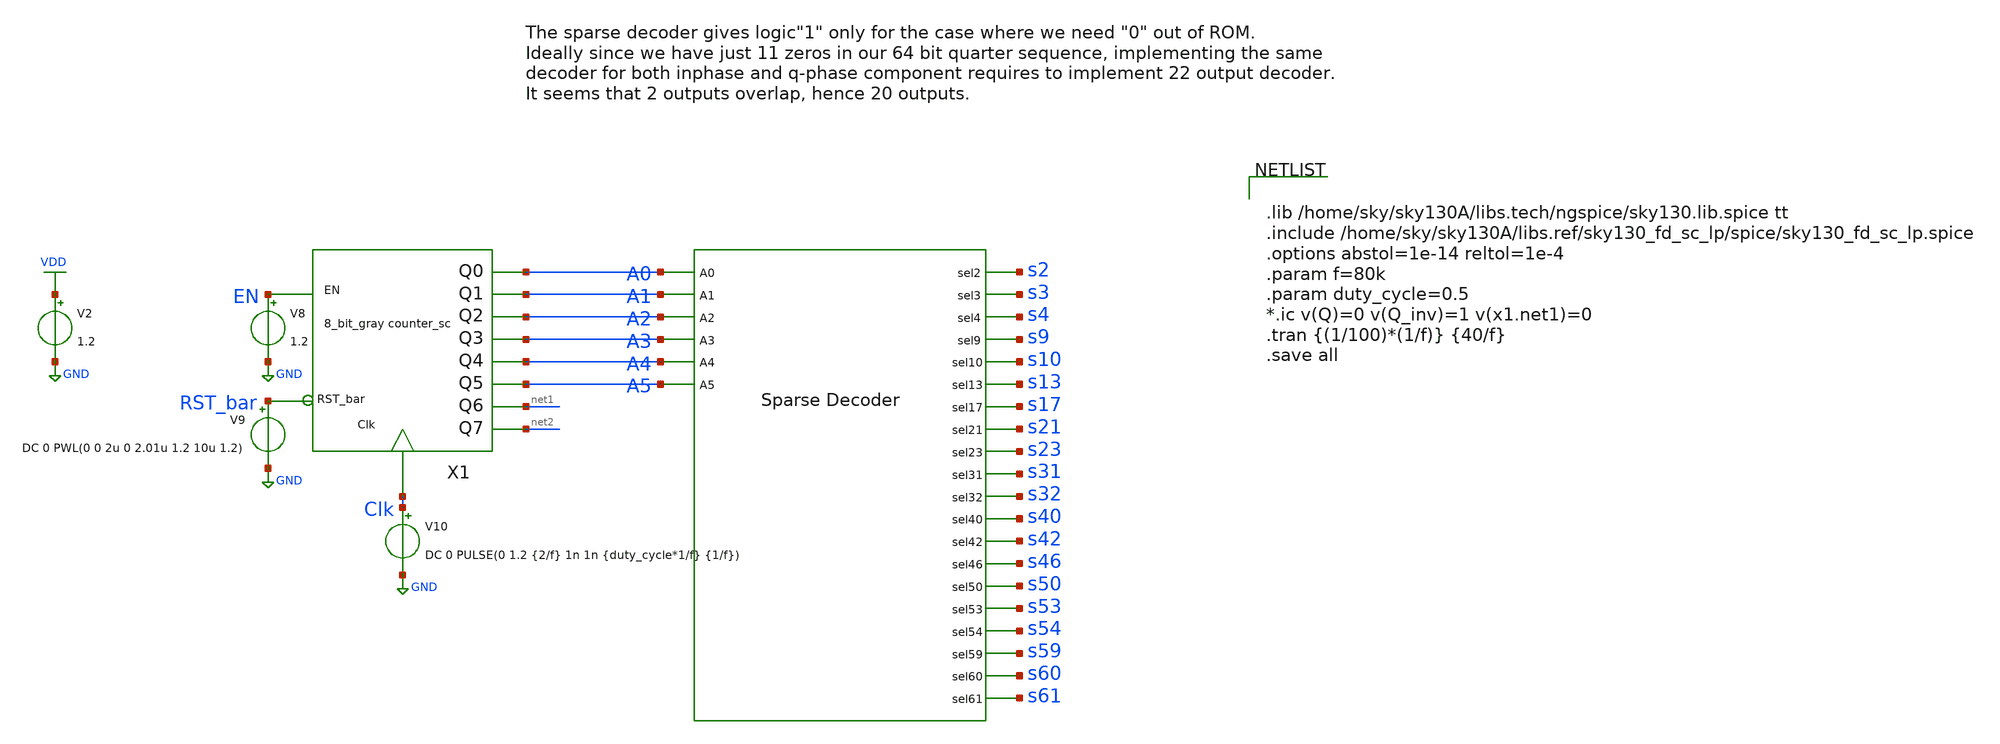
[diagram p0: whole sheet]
** sch_path: xschem/sparse_decoder/sparse_decoder_tb.sch
**.subckt sparse_decoder_tb
X1 A0 A1 A2 A3 A4 A5 s2 s3 s4 s9 s10 s13 s17 s21 s23 s31 s32 s40 s42 s46 s50 s53 s54 s59 s60 s61
+ sparse_decoder
V2 VDD GND 1.2
V8 EN GND 1.2
V9 RST_bar GND DC 0 PWL(0 0 2u 0 2.01u 1.2 10u 1.2)
V10 Clk GND DC 0 PULSE(0 1.2 {2/f} 1n 1n {duty_cycle*1/f} {1/f})
X1 EN A1 net1 Clk A0 A2 A3 A4 A5 net2 RST_bar asyn_rst_gray_counter
**** begin user architecture code


.lib /home/sky/sky130A/libs.tech/ngspice/sky130.lib.spice tt
.include /home/sky/sky130A/libs.ref/sky130_fd_sc_lp/spice/sky130_fd_sc_lp.spice
.options abstol=1e-14 reltol=1e-4
.param f=80k
.param duty_cycle=0.5
*.ic v(Q)=0 v(Q_inv)=1 v(x1.net1)=0
.tran {(1/100)*(1/f)} {40/f}
.save all


**** end user architecture code
**.ends
.GLOBAL GND
.GLOBAL VDD
.end
